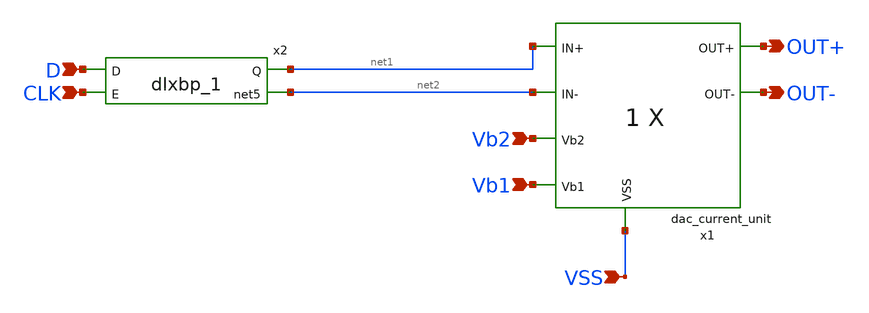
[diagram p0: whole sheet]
** sch_path: DAC/xschem/dac_current_cell.sch
**.subckt dac_current_cell VSS OUT+ OUT- Vb2 Vb1 D CLK
*.ipin VSS
*.opin OUT+
*.opin OUT-
*.ipin Vb2
*.ipin Vb1
*.ipin D
*.ipin CLK
x1 OUT+ OUT- net1 net2 Vb2 Vb1 VSS dac_current_unit nf=1
x2 D CLK net1 net2 DVDD DVNW DVPW DVSS gf180mcu_fd_sc_mcu7t5v0__latqnq_1
**.ends

* expanding   symbol:  dac_current_unit.sym # of pins=7
** sym_path: DAC/xschem/dac_current_unit.sym
** sch_path: DAC/xschem/dac_current_unit.sch
.subckt dac_current_unit OUT+ OUT- IN+ IN- Vb2 Vb1 VSS  nf=1
*.ipin IN+
*.ipin IN-
*.opin OUT-
*.opin OUT+
*.ipin Vb2
*.ipin Vb1
*.ipin VSS
XM1 net1 Vb2 net2 VSS nfet_03v3 L=0.5u W=nf*2u nf=nf ad='int((nf+1)/2) * W/nf * 0.18u' as='int((nf+2)/2) * W/nf * 0.18u'
+ pd='2*int((nf+1)/2) * (W/nf + 0.18u)' ps='2*int((nf+2)/2) * (W/nf + 0.18u)' nrd='0.18u / W' nrs='0.18u / W'
+ sa=0 sb=0 sd=0 m=1
XM2 net2 Vb1 VSS VSS nfet_03v3 L=1u W=nf*2u nf=nf ad='int((nf+1)/2) * W/nf * 0.18u' as='int((nf+2)/2) * W/nf * 0.18u'
+ pd='2*int((nf+1)/2) * (W/nf + 0.18u)' ps='2*int((nf+2)/2) * (W/nf + 0.18u)' nrd='0.18u / W' nrs='0.18u / W'
+ sa=0 sb=0 sd=0 m=1
XM5 OUT+ IN+ net1 VSS nfet_03v3 L=0.28u W=nf*1u nf=nf ad='int((nf+1)/2) * W/nf * 0.18u' as='int((nf+2)/2) * W/nf * 0.18u'
+ pd='2*int((nf+1)/2) * (W/nf + 0.18u)' ps='2*int((nf+2)/2) * (W/nf + 0.18u)' nrd='0.18u / W' nrs='0.18u / W'
+ sa=0 sb=0 sd=0 m=1
XM6 OUT- IN- net1 VSS nfet_03v3 L=0.28u W=nf*1u nf=nf ad='int((nf+1)/2) * W/nf * 0.18u' as='int((nf+2)/2) * W/nf * 0.18u'
+ pd='2*int((nf+1)/2) * (W/nf + 0.18u)' ps='2*int((nf+2)/2) * (W/nf + 0.18u)' nrd='0.18u / W' nrs='0.18u / W'
+ sa=0 sb=0 sd=0 m=1
.ends

.end
